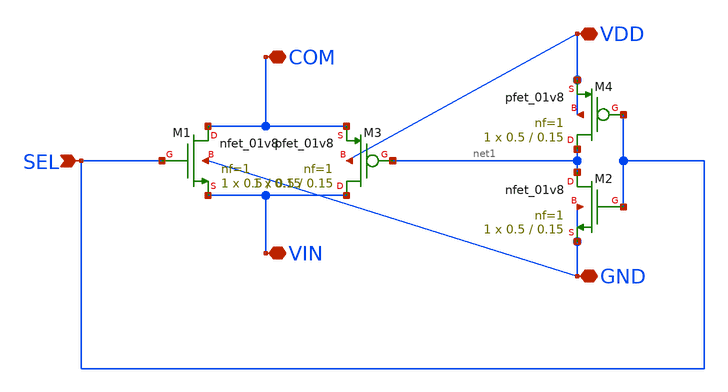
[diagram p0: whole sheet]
** sch_path: TG.sch
**.subckt TG SEL VDD GND COM VIN
*.ipin SEL
*.iopin VDD
*.iopin GND
*.iopin COM
*.iopin VIN
XM1 COM SEL VIN GND sky130_fd_pr__nfet_01v8 L=0.15 W=0.5 nf=1 ad='int((1 + 1)/2) * 0.5 / 1 * 0.29' as='int((1 + 2)/2) * 0.5 / 1 * 0.29'
+ pd='2*int((1 + 1)/2) * (0.5 / 1 + 0.29)' ps='2*int((1 + 2)/2) * (0.5 / 1 + 0.29)' nrd='0.29 / 0.5 ' nrs='0.29 / 0.5 '
+ sa=0 sb=0 sd=0 mult=1 m=1
XM2 net1 SEL GND GND sky130_fd_pr__nfet_01v8 L=0.15 W=0.5 nf=1 ad='int((1 + 1)/2) * 0.5 / 1 * 0.29' as='int((1 + 2)/2) * 0.5 / 1 * 0.29'
+ pd='2*int((1 + 1)/2) * (0.5 / 1 + 0.29)' ps='2*int((1 + 2)/2) * (0.5 / 1 + 0.29)' nrd='0.29 / 0.5 ' nrs='0.29 / 0.5 '
+ sa=0 sb=0 sd=0 mult=1 m=1
XM3 VIN net1 COM VDD sky130_fd_pr__pfet_01v8 L=0.15 W=0.5 nf=1 ad='int((1 + 1)/2) * 0.5 / 1 * 0.29' as='int((1 + 2)/2) * 0.5 / 1 * 0.29'
+ pd='2*int((1 + 1)/2) * (0.5 / 1 + 0.29)' ps='2*int((1 + 2)/2) * (0.5 / 1 + 0.29)' nrd='0.29 / 0.5 ' nrs='0.29 / 0.5 '
+ sa=0 sb=0 sd=0 mult=1 m=1
XM4 net1 SEL VDD VDD sky130_fd_pr__pfet_01v8 L=0.15 W=0.5 nf=1 ad='int((1 + 1)/2) * 0.5 / 1 * 0.29' as='int((1 + 2)/2) * 0.5 / 1 * 0.29'
+ pd='2*int((1 + 1)/2) * (0.5 / 1 + 0.29)' ps='2*int((1 + 2)/2) * (0.5 / 1 + 0.29)' nrd='0.29 / 0.5 ' nrs='0.29 / 0.5 '
+ sa=0 sb=0 sd=0 mult=1 m=1
**.ends
.end
